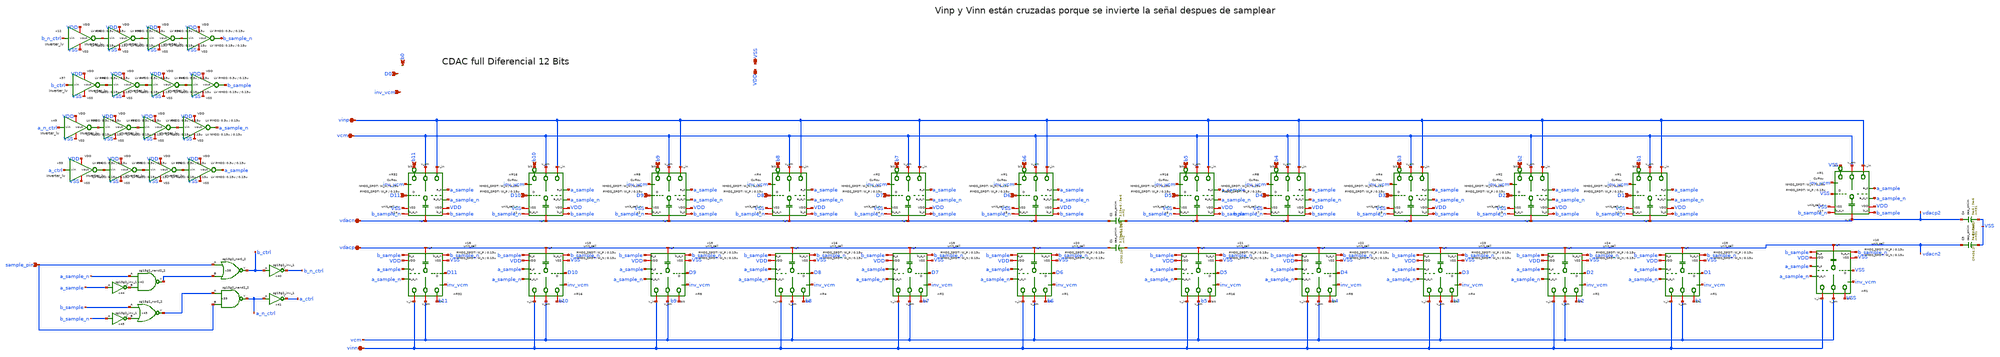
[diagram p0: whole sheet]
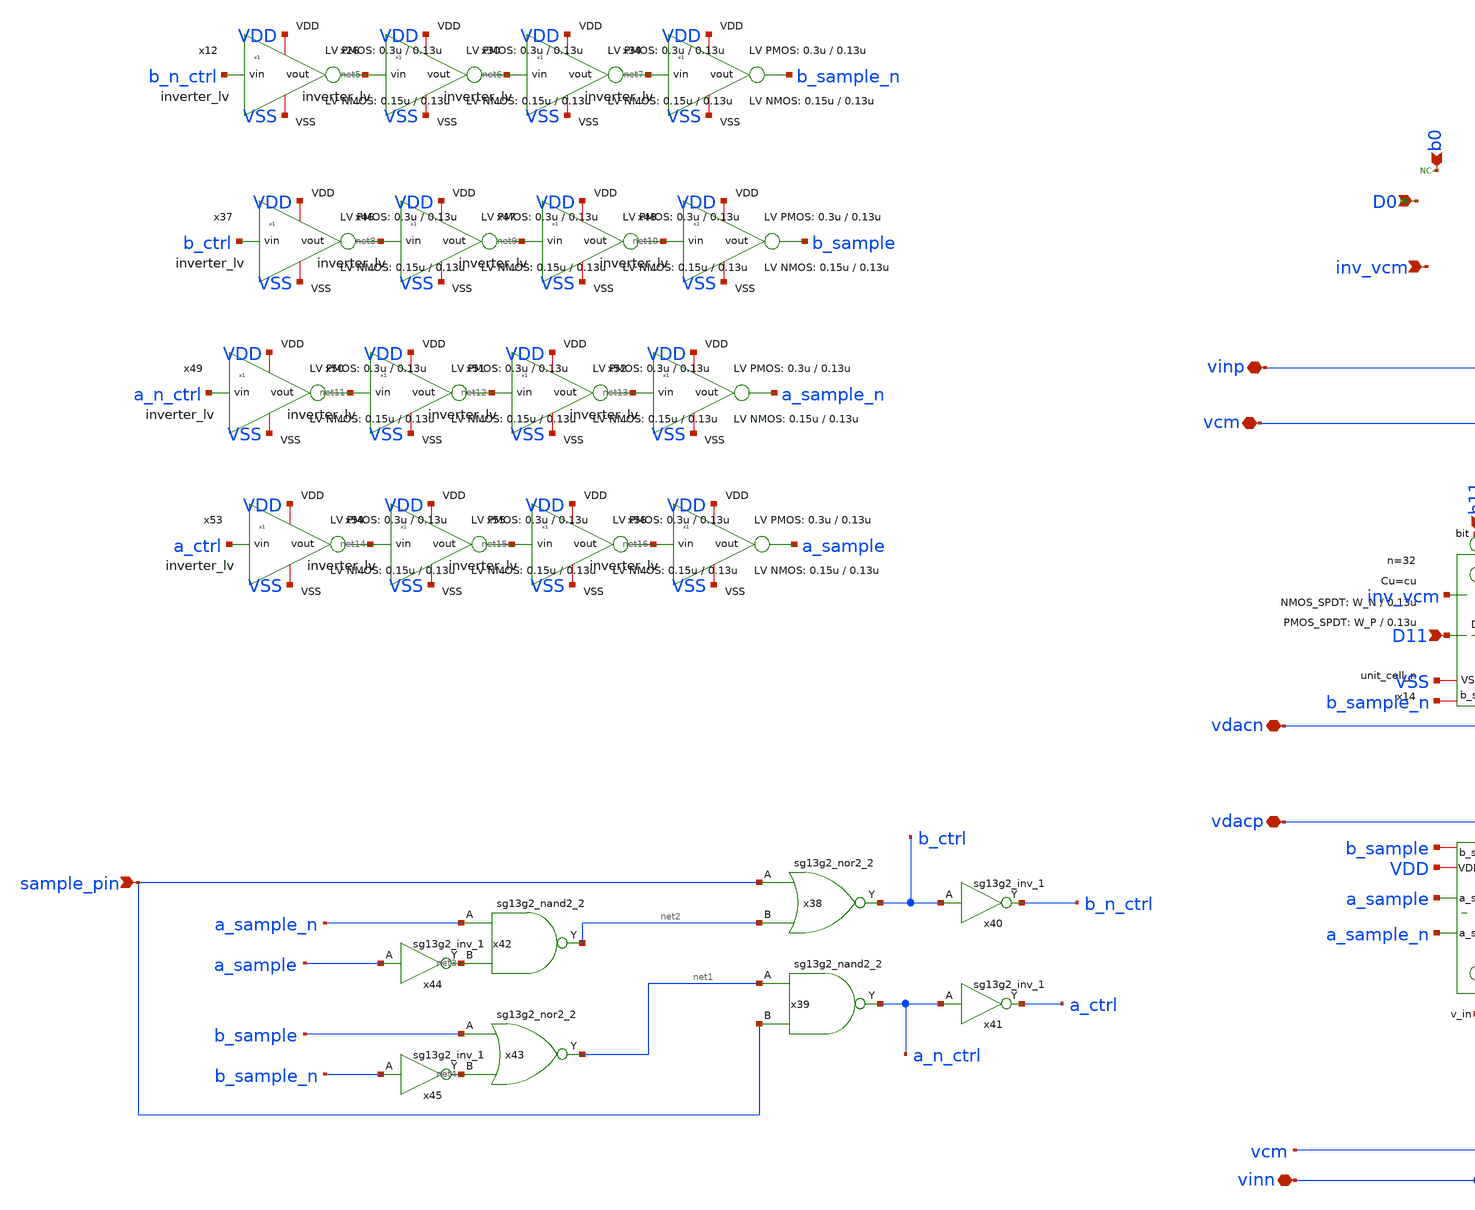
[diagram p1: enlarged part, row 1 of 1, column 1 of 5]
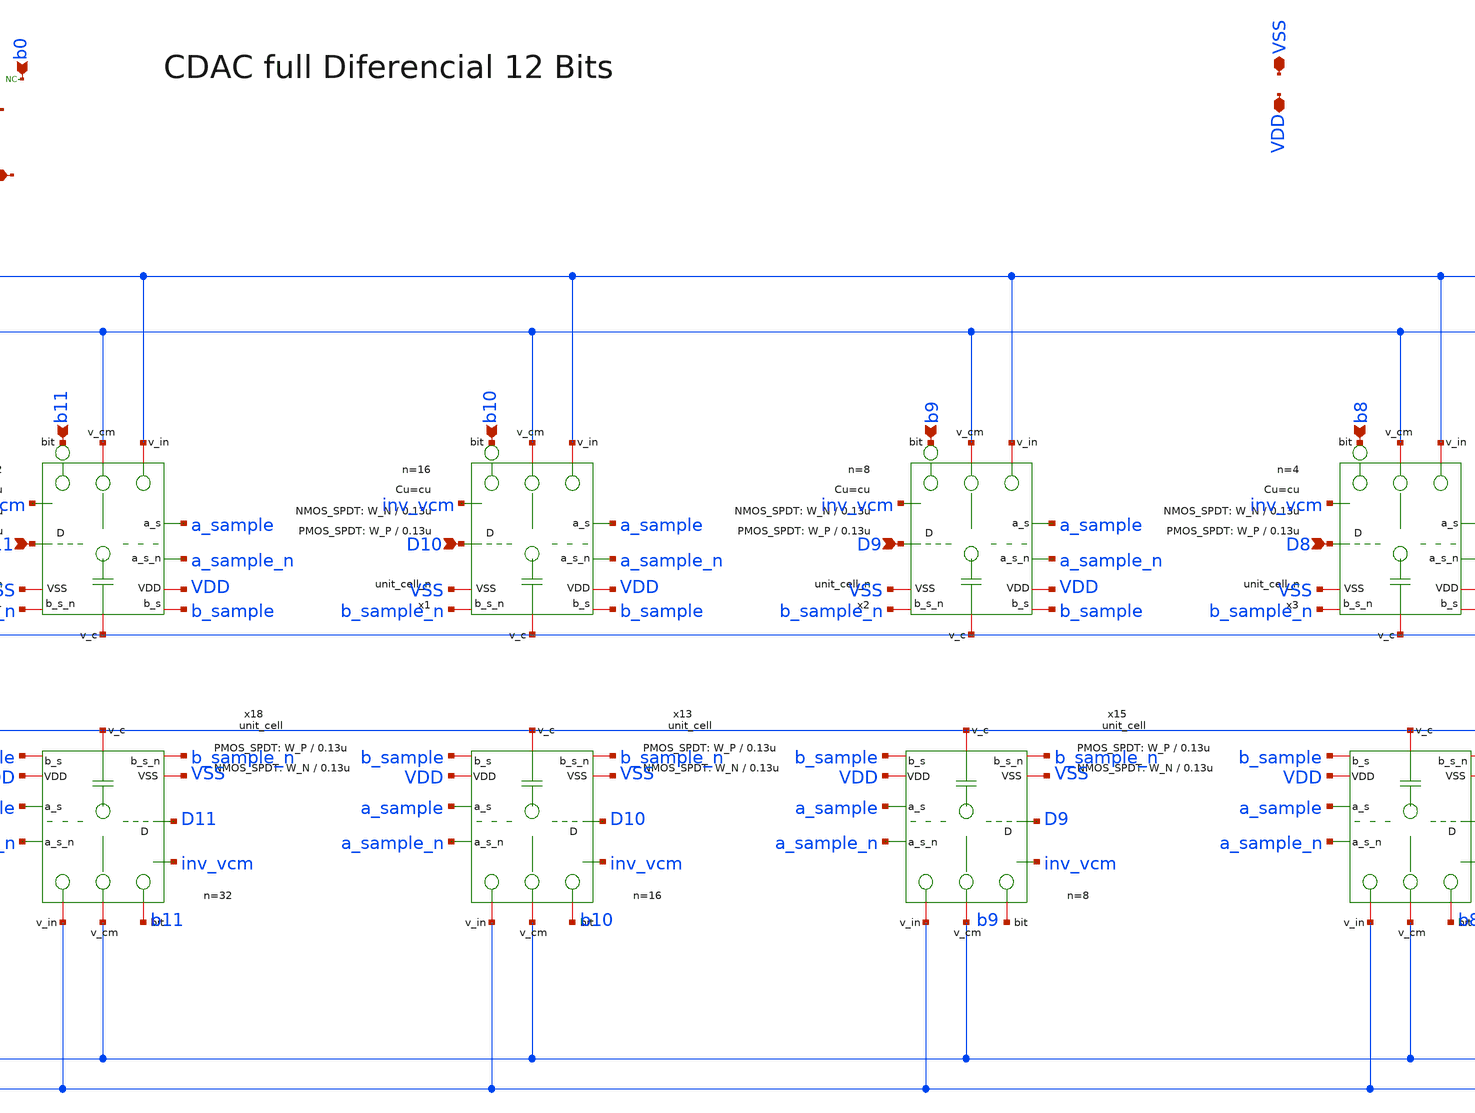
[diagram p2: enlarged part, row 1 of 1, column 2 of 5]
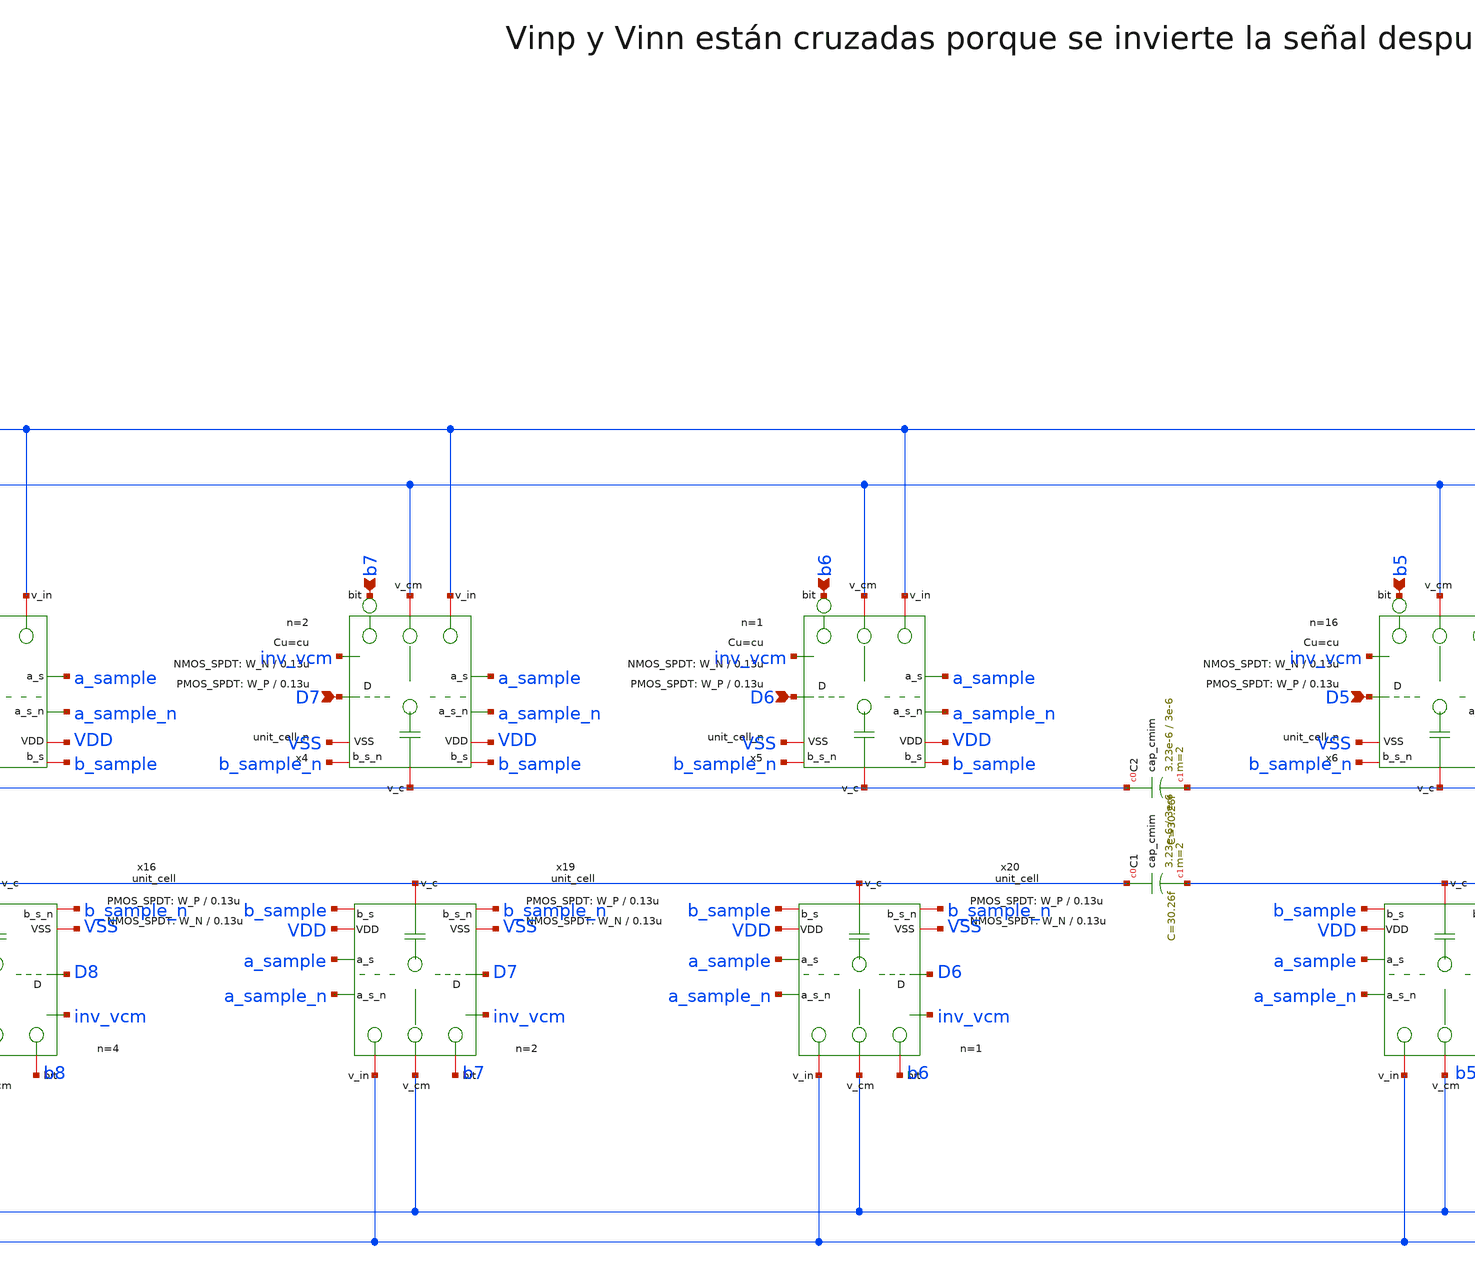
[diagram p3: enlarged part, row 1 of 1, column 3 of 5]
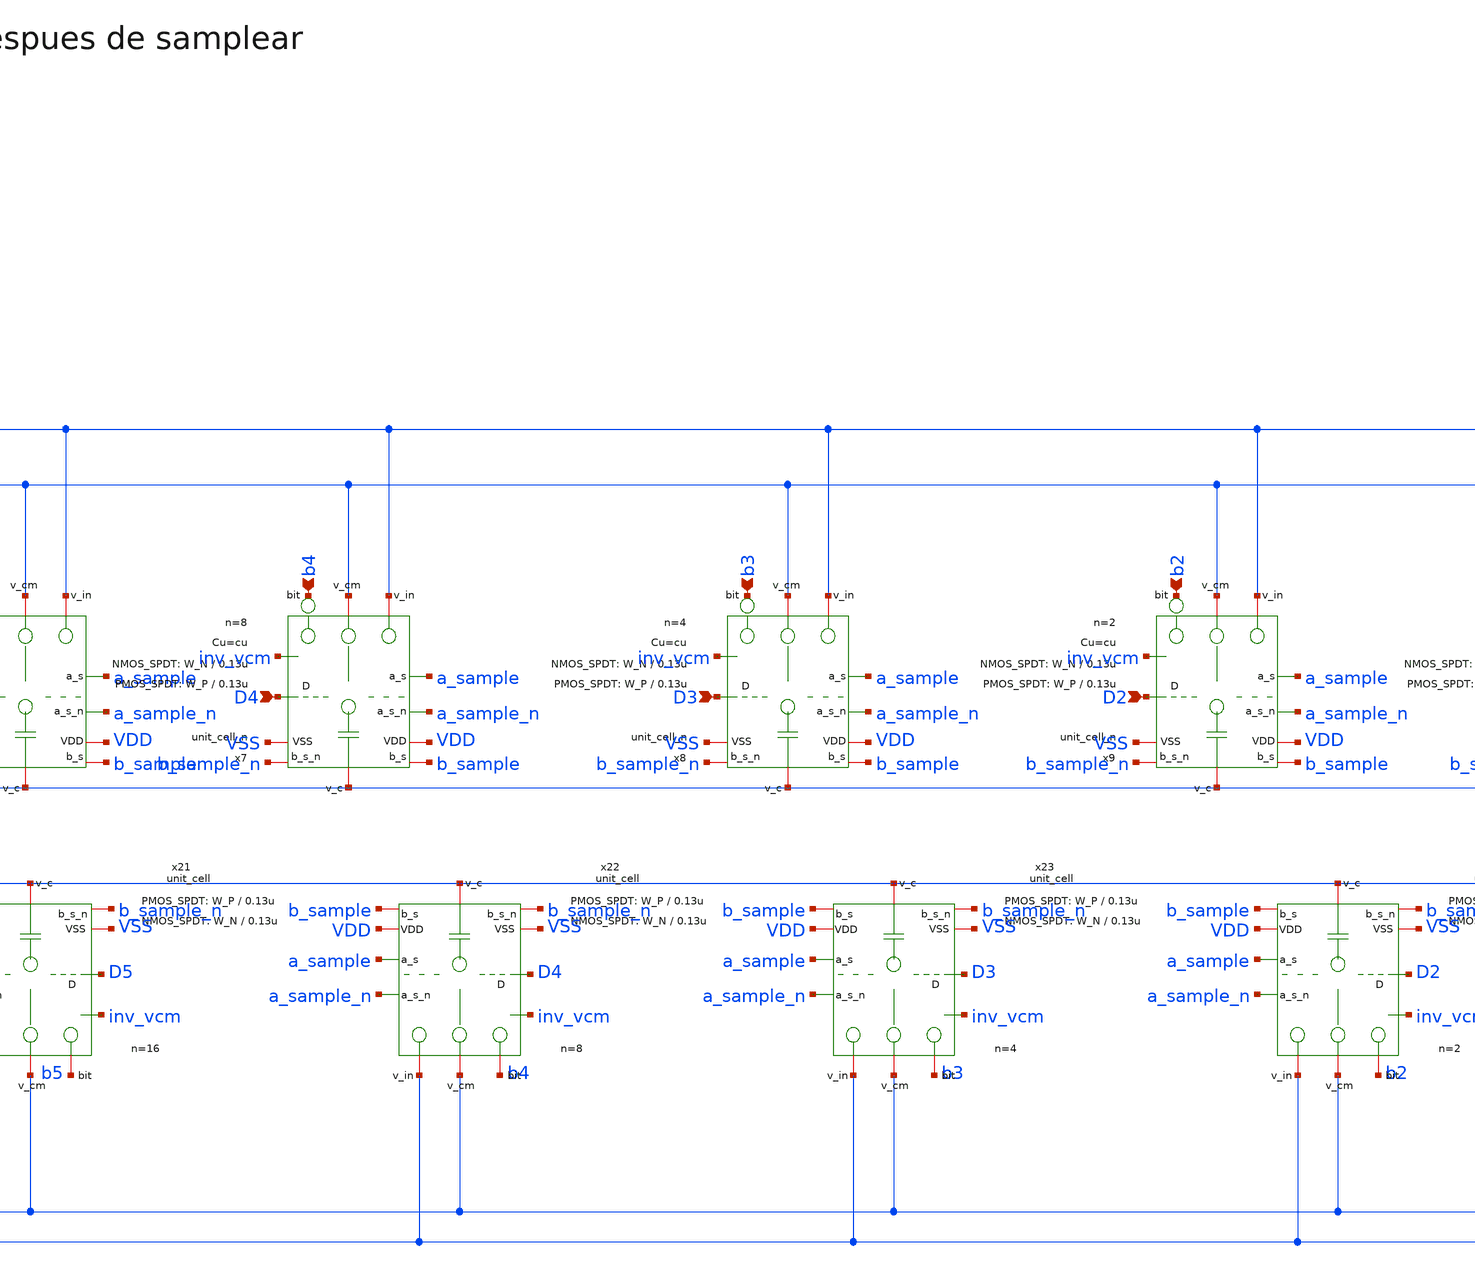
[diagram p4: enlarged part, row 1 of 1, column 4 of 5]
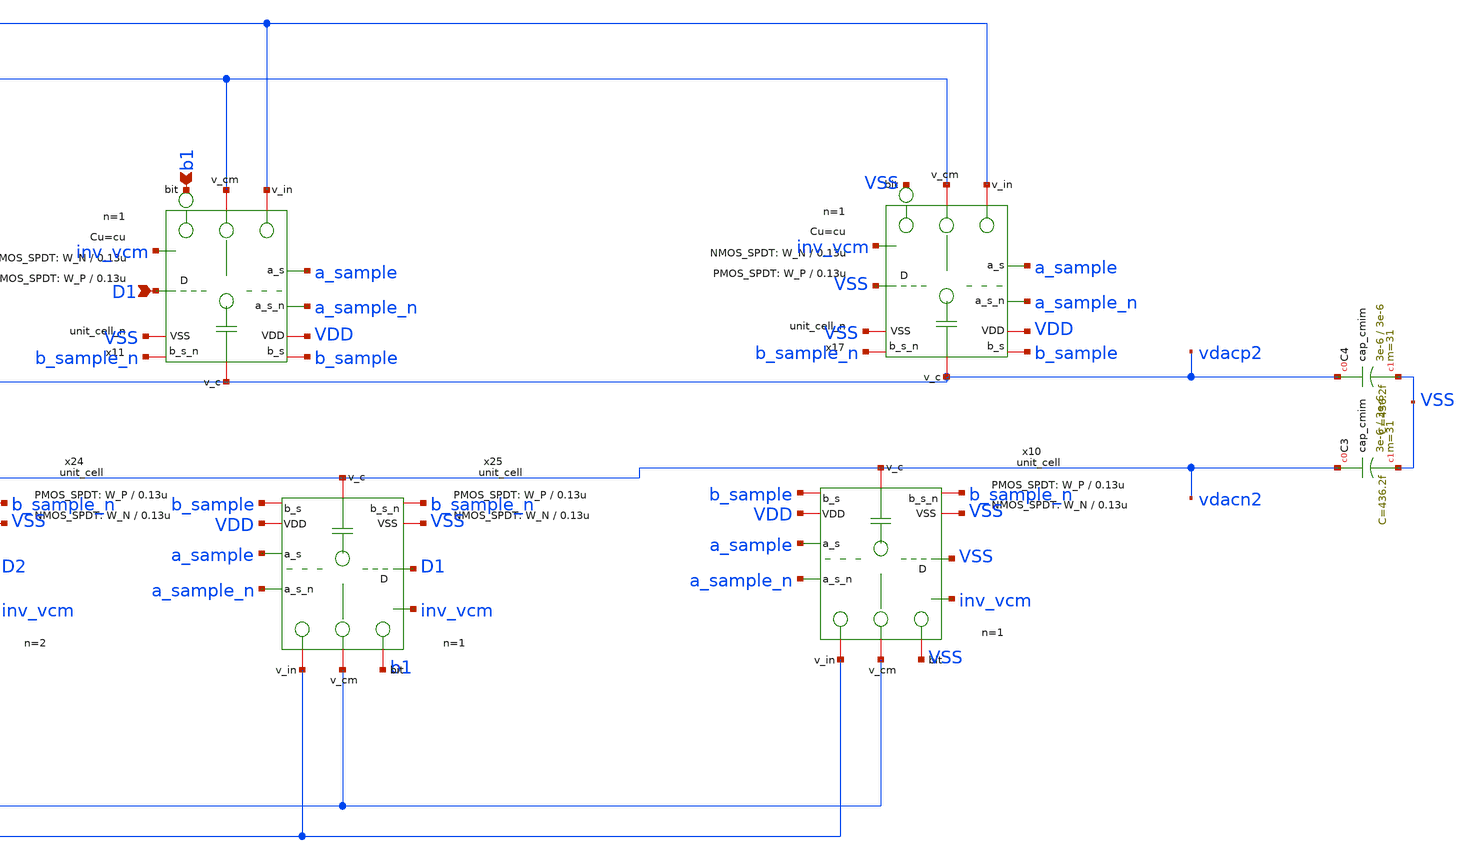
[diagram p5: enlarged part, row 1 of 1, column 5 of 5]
** sch_path: xschem/dac_icms_cell/dac.sch
* IHP-GmbH/IHP-Open-PDK/ihp-sg13g2/libs.tech/xschem/sg13g2_stdcells/sg13g2_nor2_1.sch:
* Copyright 2023 IHP PDK Authors
* Licensed under the Apache License, Version 2.0 (the "License");
**.subckt dac D0 b0 vinn vcm sample_pin vinp vdacp vdacn VSS VDD D1 b1 D2 b2 D3 b3 D4 b4 D5 b5 b6 D7
*+ b7 D8 b8 D9 b9 D10 b10 D11 b11 D6 inv_vcm
*.ipin D0
*.ipin b0
*.iopin vinn
*.iopin vcm
*.ipin sample_pin
*.iopin vinp
*.iopin vdacp
*.iopin vdacn
*.iopin VSS
*.iopin VDD
*.ipin D1
*.ipin b1
*.ipin D2
*.ipin b2
*.ipin D3
*.ipin b3
*.ipin D4
*.ipin b4
*.ipin D5
*.ipin b5
*.ipin b6
*.ipin D7
*.ipin b7
*.ipin D8
*.ipin b8
*.ipin D9
*.ipin b9
*.ipin D10
*.ipin b10
*.ipin D11
*.ipin b11
*.ipin D6
*.ipin inv_vcm
x14 VDD D11 VSS vdacn b11 vcm vinp a_sample a_sample_n b_sample b_sample_n inv_vcm unit_cell_n
+ W_P_SPDT=W_P L_P_SPDT=0.13u W_N_SPDT=W_N L_N_SPDT=0.13u Cu=cu n=32
x18 VDD D11 VSS vdacp b11 vcm vinn a_sample a_sample_n b_sample b_sample_n inv_vcm unit_cell
+ W_P_SPDT=W_P L_P_SPDT=0.13u W_N_SPDT=W_N L_N_SPDT=0.13u Cu=cu n=32
x1 VDD D10 VSS vdacn b10 vcm vinp a_sample a_sample_n b_sample b_sample_n inv_vcm unit_cell_n
+ W_P_SPDT=W_P L_P_SPDT=0.13u W_N_SPDT=W_N L_N_SPDT=0.13u Cu=cu n=16
x2 VDD D9 VSS vdacn b9 vcm vinp a_sample a_sample_n b_sample b_sample_n inv_vcm unit_cell_n
+ W_P_SPDT=W_P L_P_SPDT=0.13u W_N_SPDT=W_N L_N_SPDT=0.13u Cu=cu n=8
x3 VDD D8 VSS vdacn b8 vcm vinp a_sample a_sample_n b_sample b_sample_n inv_vcm unit_cell_n
+ W_P_SPDT=W_P L_P_SPDT=0.13u W_N_SPDT=W_N L_N_SPDT=0.13u Cu=cu n=4
x4 VDD D7 VSS vdacn b7 vcm vinp a_sample a_sample_n b_sample b_sample_n inv_vcm unit_cell_n
+ W_P_SPDT=W_P L_P_SPDT=0.13u W_N_SPDT=W_N L_N_SPDT=0.13u Cu=cu n=2
x5 VDD D6 VSS vdacn b6 vcm vinp a_sample a_sample_n b_sample b_sample_n inv_vcm unit_cell_n
+ W_P_SPDT=W_P L_P_SPDT=0.13u W_N_SPDT=W_N L_N_SPDT=0.13u Cu=cu n=1
x6 VDD D5 VSS vdacp2 b5 vcm vinp a_sample a_sample_n b_sample b_sample_n inv_vcm unit_cell_n
+ W_P_SPDT=W_P L_P_SPDT=0.13u W_N_SPDT=W_N L_N_SPDT=0.13u Cu=cu n=16
x7 VDD D4 VSS vdacp2 b4 vcm vinp a_sample a_sample_n b_sample b_sample_n inv_vcm unit_cell_n
+ W_P_SPDT=W_P L_P_SPDT=0.13u W_N_SPDT=W_N L_N_SPDT=0.13u Cu=cu n=8
x8 VDD D3 VSS vdacp2 b3 vcm vinp a_sample a_sample_n b_sample b_sample_n inv_vcm unit_cell_n
+ W_P_SPDT=W_P L_P_SPDT=0.13u W_N_SPDT=W_N L_N_SPDT=0.13u Cu=cu n=4
x9 VDD D2 VSS vdacp2 b2 vcm vinp a_sample a_sample_n b_sample b_sample_n inv_vcm unit_cell_n
+ W_P_SPDT=W_P L_P_SPDT=0.13u W_N_SPDT=W_N L_N_SPDT=0.13u Cu=cu n=2
x11 VDD D1 VSS vdacp2 b1 vcm vinp a_sample a_sample_n b_sample b_sample_n inv_vcm unit_cell_n
+ W_P_SPDT=W_P L_P_SPDT=0.13u W_N_SPDT=W_N L_N_SPDT=0.13u Cu=cu n=1
x13 VDD D10 VSS vdacp b10 vcm vinn a_sample a_sample_n b_sample b_sample_n inv_vcm unit_cell
+ W_P_SPDT=W_P L_P_SPDT=0.13u W_N_SPDT=W_N L_N_SPDT=0.13u Cu=cu n=16
x15 VDD D9 VSS vdacp b9 vcm vinn a_sample a_sample_n b_sample b_sample_n inv_vcm unit_cell
+ W_P_SPDT=W_P L_P_SPDT=0.13u W_N_SPDT=W_N L_N_SPDT=0.13u Cu=cu n=8
x16 VDD D8 VSS vdacp b8 vcm vinn a_sample a_sample_n b_sample b_sample_n inv_vcm unit_cell
+ W_P_SPDT=W_P L_P_SPDT=0.13u W_N_SPDT=W_N L_N_SPDT=0.13u Cu=cu n=4
x19 VDD D7 VSS vdacp b7 vcm vinn a_sample a_sample_n b_sample b_sample_n inv_vcm unit_cell
+ W_P_SPDT=W_P L_P_SPDT=0.13u W_N_SPDT=W_N L_N_SPDT=0.13u Cu=cu n=2
x20 VDD D6 VSS vdacp b6 vcm vinn a_sample a_sample_n b_sample b_sample_n inv_vcm unit_cell
+ W_P_SPDT=W_P L_P_SPDT=0.13u W_N_SPDT=W_N L_N_SPDT=0.13u Cu=cu n=1
x21 VDD D5 VSS vdacn2 b5 vcm vinn a_sample a_sample_n b_sample b_sample_n inv_vcm unit_cell
+ W_P_SPDT=W_P L_P_SPDT=0.13u W_N_SPDT=W_N L_N_SPDT=0.13u Cu=cu n=16
x22 VDD D4 VSS vdacn2 b4 vcm vinn a_sample a_sample_n b_sample b_sample_n inv_vcm unit_cell
+ W_P_SPDT=W_P L_P_SPDT=0.13u W_N_SPDT=W_N L_N_SPDT=0.13u Cu=cu n=8
x23 VDD D3 VSS vdacn2 b3 vcm vinn a_sample a_sample_n b_sample b_sample_n inv_vcm unit_cell
+ W_P_SPDT=W_P L_P_SPDT=0.13u W_N_SPDT=W_N L_N_SPDT=0.13u Cu=cu n=4
x24 VDD D2 VSS vdacn2 b2 vcm vinn a_sample a_sample_n b_sample b_sample_n inv_vcm unit_cell
+ W_P_SPDT=W_P L_P_SPDT=0.13u W_N_SPDT=W_N L_N_SPDT=0.13u Cu=cu n=2
x25 VDD D1 VSS vdacn2 b1 vcm vinn a_sample a_sample_n b_sample b_sample_n inv_vcm unit_cell
+ W_P_SPDT=W_P L_P_SPDT=0.13u W_N_SPDT=W_N L_N_SPDT=0.13u Cu=cu n=1
x38 b_ctrl sample_pin net2 VDD VSS sg13g2_nor2_2
x39 a_n_ctrl net1 sample_pin VDD VSS sg13g2_nand2_2
x40 b_n_ctrl b_ctrl VDD VSS sg13g2_inv_1
x41 a_ctrl a_n_ctrl VDD VSS sg13g2_inv_1
x42 net2 a_sample_n net3 VDD VSS sg13g2_nand2_2
x43 net1 b_sample net4 VDD VSS sg13g2_nor2_2
x44 net3 a_sample VDD VSS sg13g2_inv_1
x45 net4 b_sample_n VDD VSS sg13g2_inv_1
XC1 vdacp vdacn2 cap_cmim w=3.23e-6 l=3e-6 m=2 mm_ok=1
XC2 vdacn vdacp2 cap_cmim w=3.23e-6 l=3e-6 m=2 mm_ok=1
x10 VDD VSS VSS vdacn2 VSS vcm vinn a_sample a_sample_n b_sample b_sample_n inv_vcm unit_cell
+ W_P_SPDT=W_P L_P_SPDT=0.13u W_N_SPDT=W_N L_N_SPDT=0.13u Cu=cu n=1
x17 VDD VSS VSS vdacp2 VSS vcm vinp a_sample a_sample_n b_sample b_sample_n inv_vcm unit_cell_n
+ W_P_SPDT=W_P L_P_SPDT=0.13u W_N_SPDT=W_N L_N_SPDT=0.13u Cu=cu n=1
XC3 vdacn2 VSS cap_cmim w=3e-6 l=3e-6 m=31 mm_ok=1
XC4 vdacp2 VSS cap_cmim w=3e-6 l=3e-6 m=31 mm_ok=1
* noconn b0
* noconn D0
x12 VDD b_n_ctrl net5 VSS inverter_lv W_P=0.3u L_P=0.13u W_N=0.15u L_N=0.13u N_C=1
x26 VDD net5 net6 VSS inverter_lv W_P=0.3u L_P=0.13u W_N=0.15u L_N=0.13u N_C=1
x30 VDD net6 net7 VSS inverter_lv W_P=0.3u L_P=0.13u W_N=0.15u L_N=0.13u N_C=1
x34 VDD net7 b_sample_n VSS inverter_lv W_P=0.3u L_P=0.13u W_N=0.15u L_N=0.13u N_C=1
x37 VDD b_ctrl net8 VSS inverter_lv W_P=0.3u L_P=0.13u W_N=0.15u L_N=0.13u N_C=1
x46 VDD net8 net9 VSS inverter_lv W_P=0.3u L_P=0.13u W_N=0.15u L_N=0.13u N_C=1
x47 VDD net9 net10 VSS inverter_lv W_P=0.3u L_P=0.13u W_N=0.15u L_N=0.13u N_C=1
x48 VDD net10 b_sample VSS inverter_lv W_P=0.3u L_P=0.13u W_N=0.15u L_N=0.13u N_C=1
x49 VDD a_n_ctrl net11 VSS inverter_lv W_P=0.3u L_P=0.13u W_N=0.15u L_N=0.13u N_C=1
x50 VDD net11 net12 VSS inverter_lv W_P=0.3u L_P=0.13u W_N=0.15u L_N=0.13u N_C=1
x51 VDD net12 net13 VSS inverter_lv W_P=0.3u L_P=0.13u W_N=0.15u L_N=0.13u N_C=1
x52 VDD net13 a_sample_n VSS inverter_lv W_P=0.3u L_P=0.13u W_N=0.15u L_N=0.13u N_C=1
x53 VDD a_ctrl net14 VSS inverter_lv W_P=0.3u L_P=0.13u W_N=0.15u L_N=0.13u N_C=1
x54 VDD net14 net15 VSS inverter_lv W_P=0.3u L_P=0.13u W_N=0.15u L_N=0.13u N_C=1
x55 VDD net15 net16 VSS inverter_lv W_P=0.3u L_P=0.13u W_N=0.15u L_N=0.13u N_C=1
x56 VDD net16 a_sample VSS inverter_lv W_P=0.3u L_P=0.13u W_N=0.15u L_N=0.13u N_C=1
**.ends

* expanding   symbol:  dac_icms_cell/unit_cell_n.sym # of pins=12
** sym_path: xschem/dac_icms_cell/unit_cell_n.sym
** sch_path: xschem/dac_icms_cell/unit_cell_n.sch
.subckt unit_cell_n VDD d VSS v_top bit v_cm v_in a_sample a_sample_n b_sample b_sample_n inv_vcm
+  W_P_SPDT=1.0u L_P_SPDT=0.13u W_N_SPDT=1.0u L_N_SPDT=0.13u Cu=8f n=1
*.iopin v_top
*.ipin a_sample
*.ipin a_sample_n
*.ipin b_sample
*.ipin b_sample_n
*.iopin v_in
*.ipin d
*.iopin v_cm
*.ipin bit
*.ipin inv_vcm
*.iopin VSS
*.iopin VDD
x2 VDD a_sample VSS v_top v_cm a_sample_n transmission_gate_lv_wo_dummy W_P=W_P_SPDT L_P=L_P_SPDT
+ W_N=W_N_SPDT L_N=L_N_SPDT W_P_D=1.0u L_P_D=0.13u W_N_D=1.0u L_N_D=0.13u n=n
XC1 TOP_C v_top cap_cmim w=3e-6 l=3e-6 m=n mm_ok=1
XM1 TOP_C n_ctrl VSS VSS sg13_lv_nmos w=1u l=0.13u ng=1 m=n mm_ok=1
XM3 TOP_C p_ctrl VDD VDD sg13_lv_pmos w=2u l=0.13u ng=1 m=n mm_ok=1
x3 VDD tg_vcm_ctrl VSS TOP_C v_cm tg_vcm_ctrl_n transmission_gate_lv_wo_dummy W_P=W_P_SPDT
+ L_P=L_P_SPDT W_N=W_N_SPDT L_N=L_N_SPDT W_P_D=1.0u L_P_D=0.13u W_N_D=1.0u L_N_D=0.13u n=n
x4 VDD b_sample_n VSS TOP_C v_in b_sample transmission_gate_lv_w_dummy W_P=W_P_SPDT L_P=L_P_SPDT
+ W_N=W_N_SPDT L_N=L_N_SPDT W_P_D=1.0u L_P_D=0.13u W_N_D=1.0u L_N_D=0.13u n=n
x23 p_ctrl_1 bit d VDD VSS sg13g2_and2_1
x46 n_ctrl_1 bit_n d VDD VSS sg13g2_nand2_1
x32 bit_n bit VDD VSS sg13g2_inv_1
x1 tg_vcm_ctrl_1 d b_sample_n VDD VSS sg13g2_or2_1
x8 tg_vcm_ctrl_n_1 d b_sample_n VDD VSS sg13g2_nor2_1
x10 VDD p_ctrl_2 p_ctrl_3 VSS inverter_lv W_P=0.3u L_P=0.13u W_N=0.15u L_N=0.13u N_C=1
x5 VDD p_ctrl_1 p_ctrl_2 VSS inverter_lv W_P=0.3u L_P=0.13u W_N=0.15u L_N=0.13u N_C=1
x6 VDD p_ctrl_3 p_ctrl VSS inverter_lv W_P=0.3u L_P=0.13u W_N=0.15u L_N=0.13u N_C=1
x11 VDD n_ctrl_2 n_ctrl_3 VSS inverter_lv W_P=0.3u L_P=0.13u W_N=0.15u L_N=0.13u N_C=1
x12 VDD n_ctrl_1 n_ctrl_2 VSS inverter_lv W_P=0.3u L_P=0.13u W_N=0.15u L_N=0.13u N_C=1
x13 VDD n_ctrl_3 n_ctrl VSS inverter_lv W_P=0.3u L_P=0.13u W_N=0.15u L_N=0.13u N_C=1
x7 VDD tg_vcm_ctrl_2 tg_vcm_ctrl_3 VSS inverter_lv W_P=0.3u L_P=0.13u W_N=0.15u L_N=0.13u N_C=1
x9 VDD tg_vcm_ctrl_1 tg_vcm_ctrl_2 VSS inverter_lv W_P=0.3u L_P=0.13u W_N=0.15u L_N=0.13u N_C=1
x14 VDD tg_vcm_ctrl_3 tg_vcm_ctrl VSS inverter_lv W_P=0.3u L_P=0.13u W_N=0.15u L_N=0.13u N_C=1
x15 VDD tg_vcm_ctrl_n_2 tg_vcm_ctrl_n_3 VSS inverter_lv W_P=0.3u L_P=0.13u W_N=0.15u L_N=0.13u N_C=1
x16 VDD tg_vcm_ctrl_n_1 tg_vcm_ctrl_n_2 VSS inverter_lv W_P=0.3u L_P=0.13u W_N=0.15u L_N=0.13u N_C=1
x17 VDD tg_vcm_ctrl_n_3 tg_vcm_ctrl_n VSS inverter_lv W_P=0.3u L_P=0.13u W_N=0.15u L_N=0.13u N_C=1
.ends


* expanding   symbol:  dac_icms_cell/unit_cell.sym # of pins=12
** sym_path: xschem/dac_icms_cell/unit_cell.sym
** sch_path: xschem/dac_icms_cell/unit_cell.sch
.subckt unit_cell VDD d VSS v_top bit v_cm v_in a_sample a_sample_n b_sample b_sample_n inv_vcm
+  W_P_SPDT=1.0u L_P_SPDT=0.13u W_N_SPDT=1.0u L_N_SPDT=0.13u Cu=8f n=1
*.iopin v_top
*.ipin a_sample
*.ipin a_sample_n
*.ipin b_sample
*.ipin b_sample_n
*.iopin v_in
*.ipin d
*.iopin v_cm
*.ipin bit
*.ipin inv_vcm
*.iopin VSS
*.iopin VDD
x2 VDD a_sample VSS v_top v_cm a_sample_n transmission_gate_lv_wo_dummy W_P=W_P_SPDT L_P=L_P_SPDT
+ W_N=W_N_SPDT L_N=L_N_SPDT W_P_D=1.0u L_P_D=0.13u W_N_D=1.0u L_N_D=0.13u n=n
XC1 TOP_C v_top cap_cmim w=3e-6 l=3e-6 m=n mm_ok=1
XM1 TOP_C n_ctrl VSS VSS sg13_lv_nmos w=1u l=0.13u ng=1 m=n mm_ok=1
XM3 TOP_C p_ctrl VDD VDD sg13_lv_pmos w=2u l=0.13u ng=1 m=n mm_ok=1
x3 VDD tg_vcm_ctrl VSS TOP_C v_cm tg_vcm_ctrl_n transmission_gate_lv_wo_dummy W_P=W_P_SPDT
+ L_P=L_P_SPDT W_N=W_N_SPDT L_N=L_N_SPDT W_P_D=1.0u L_P_D=0.13u W_N_D=1.0u L_N_D=0.13u n=n
x4 VDD b_sample_n VSS TOP_C v_in b_sample transmission_gate_lv_w_dummy W_P=W_P_SPDT L_P=L_P_SPDT
+ W_N=W_N_SPDT L_N=L_N_SPDT W_P_D=1.0u L_P_D=0.13u W_N_D=1.0u L_N_D=0.13u n=n
x23 p_ctrl_1 bit_n d VDD VSS sg13g2_and2_1
x46 n_ctrl_1 bit d VDD VSS sg13g2_nand2_1
x32 bit_n bit VDD VSS sg13g2_inv_1
x1 tg_vcm_ctrl_1 d b_sample_n VDD VSS sg13g2_or2_1
x8 tg_vcm_ctrl_n_1 d b_sample_n VDD VSS sg13g2_nor2_1
x10 VDD p_ctrl_2 p_ctrl_3 VSS inverter_lv W_P=0.3u L_P=0.13u W_N=0.15u L_N=0.13u N_C=1
x5 VDD p_ctrl_1 p_ctrl_2 VSS inverter_lv W_P=0.3u L_P=0.13u W_N=0.15u L_N=0.13u N_C=1
x6 VDD p_ctrl_3 p_ctrl VSS inverter_lv W_P=0.3u L_P=0.13u W_N=0.15u L_N=0.13u N_C=1
x11 VDD n_ctrl_2 n_ctrl_3 VSS inverter_lv W_P=0.3u L_P=0.13u W_N=0.15u L_N=0.13u N_C=1
x12 VDD n_ctrl_1 n_ctrl_2 VSS inverter_lv W_P=0.3u L_P=0.13u W_N=0.15u L_N=0.13u N_C=1
x13 VDD n_ctrl_3 n_ctrl VSS inverter_lv W_P=0.3u L_P=0.13u W_N=0.15u L_N=0.13u N_C=1
x7 VDD tg_vcm_ctrl_2 tg_vcm_ctrl_3 VSS inverter_lv W_P=0.3u L_P=0.13u W_N=0.15u L_N=0.13u N_C=1
x9 VDD tg_vcm_ctrl_1 tg_vcm_ctrl_2 VSS inverter_lv W_P=0.3u L_P=0.13u W_N=0.15u L_N=0.13u N_C=1
x14 VDD tg_vcm_ctrl_3 tg_vcm_ctrl VSS inverter_lv W_P=0.3u L_P=0.13u W_N=0.15u L_N=0.13u N_C=1
x15 VDD tg_vcm_ctrl_n_2 tg_vcm_ctrl_n_3 VSS inverter_lv W_P=0.3u L_P=0.13u W_N=0.15u L_N=0.13u N_C=1
x16 VDD tg_vcm_ctrl_n_1 tg_vcm_ctrl_n_2 VSS inverter_lv W_P=0.3u L_P=0.13u W_N=0.15u L_N=0.13u N_C=1
x17 VDD tg_vcm_ctrl_n_3 tg_vcm_ctrl_n VSS inverter_lv W_P=0.3u L_P=0.13u W_N=0.15u L_N=0.13u N_C=1
.ends


* expanding   symbol:  sg13g2_stdcells/sg13g2_nor2_2.sym # of pins=3
** sym_path: sg13g2_stdcells/sg13g2_nor2_2.sym
** sch_path: sg13g2_stdcells/sg13g2_nor2_2.sch
.subckt sg13g2_nor2_2 Y A B VDD VSS
*.opin Y
*.ipin B
*.ipin A
*.iopin VDD
*.iopin VSS
XM1 Y A VSS VSS sg13_lv_nmos w=1.48u l=130.00n ng=2 m=1 mm_ok=1
XM2 Y B VSS VSS sg13_lv_nmos w=1.48u l=130.00n ng=2 m=1 mm_ok=1
XM3 net1 A VDD VDD sg13_lv_pmos w=2.24u l=130.00n ng=2 m=1 mm_ok=1
XM4 Y B net1 VDD sg13_lv_pmos w=2.24u l=130.00n ng=2 m=1 mm_ok=1
.ends


* expanding   symbol:  sg13g2_stdcells/sg13g2_nand2_2.sym # of pins=3
** sym_path: sg13g2_stdcells/sg13g2_nand2_2.sym
** sch_path: sg13g2_stdcells/sg13g2_nand2_2.sch
.subckt sg13g2_nand2_2 Y A B VDD VSS
*.iopin VDD
*.iopin VSS
*.opin Y
*.ipin B
*.ipin A
XM1 Y A net1 VSS sg13_lv_nmos w=1.44u l=130.00n ng=2 m=1 mm_ok=1
XM2 net1 B VSS VSS sg13_lv_nmos w=1.44u l=130.00n ng=2 m=1 mm_ok=1
XM3 Y A VDD VDD sg13_lv_pmos w=2.24u l=130.00n ng=2 m=1 mm_ok=1
XM4 Y B VDD VDD sg13_lv_pmos w=2.24u l=130.00n ng=2 m=1 mm_ok=1
.ends


* expanding   symbol:  sg13g2_stdcells/sg13g2_inv_1.sym # of pins=2
** sym_path: sg13g2_stdcells/sg13g2_inv_1.sym
** sch_path: sg13g2_stdcells/sg13g2_inv_1.sch
.subckt sg13g2_inv_1 Y A VDD VSS
*.opin Y
*.ipin A
*.iopin VDD
*.iopin VSS
XM1 Y A VSS VSS sg13_lv_nmos w=740.00n l=130.00n ng=1 m=1 mm_ok=1
XM2 Y A VDD VDD sg13_lv_pmos w=1.12u l=130.00n ng=1 m=1 mm_ok=1
.ends


* expanding   symbol:  inverter/inverter_lv.sym # of pins=4
** sym_path: xschem/inverter/inverter_lv.sym
** sch_path: xschem/inverter/inverter_lv.sch
.subckt inverter_lv VDD vin vout VSS  W_P=3.0u L_P=0.13u W_N=1.0u L_N=0.13u N_C=1
*.ipin vin
*.iopin VDD
*.iopin VSS
*.opin vout
XM1 vout vin VDD VDD sg13_lv_pmos w=W_P l=L_P ng=1 m={N_C} mm_ok=1
XM2 vout vin VSS VSS sg13_lv_nmos w=W_N l=L_N ng=1 m={N_C} mm_ok=1
.ends


* expanding   symbol:  transmission_gate/transmission_gate_lv_wo_dummy.sym # of pins=6
** sym_path: xschem/transmission_gate/transmission_gate_lv_wo_dummy.sym
** sch_path: xschem/transmission_gate/transmission_gate_lv_wo_dummy.sch
.subckt transmission_gate_lv_wo_dummy VDD di_tg_ctrl VSS v_b v_a di_tg_ctrl_n  W_P=2.0u L_P=0.13u
+ W_N=2.0u L_N=0.13u W_P_D=1.0u L_P_D=0.13u W_N_D=1.0u L_N_D=0.13u n=1
*.iopin v_a
*.iopin v_b
*.iopin VDD
*.iopin VSS
*.ipin di_tg_ctrl
*.ipin di_tg_ctrl_n
XM1 v_a di_tg_ctrl v_b VSS sg13_lv_nmos w=W_N l=L_N ng=1 m=n mm_ok=1
XM2 v_a di_tg_ctrl_n v_b VDD sg13_lv_pmos w=W_P l=L_P ng=1 m=n mm_ok=1
.ends


* expanding   symbol:  transmission_gate/transmission_gate_lv_w_dummy.sym # of pins=6
** sym_path: xschem/transmission_gate/transmission_gate_lv_w_dummy.sym
** sch_path: xschem/transmission_gate/transmission_gate_lv_w_dummy.sch
.subckt transmission_gate_lv_w_dummy VDD di_tg_ctrl VSS v_b v_a di_tg_ctrl_n  W_P=2.0u L_P=0.13u
+ W_N=2.0u L_N=0.13u W_P_D=1.0u L_P_D=0.13u W_N_D=1.0u L_N_D=0.13u n=1
*.iopin v_a
*.iopin v_b
*.iopin VDD
*.iopin VSS
*.ipin di_tg_ctrl
*.ipin di_tg_ctrl_n
XM1 v_a di_tg_ctrl v_b VSS sg13_lv_nmos w=W_N l=L_N ng=1 m=n mm_ok=1
XM2 v_a di_tg_ctrl_n v_b VDD sg13_lv_pmos w=W_P l=L_P ng=1 m=n mm_ok=1
XMdummy2 v_b di_tg_ctrl v_b VDD sg13_lv_pmos w=W_P l=L_P ng=1 m={n/2} mm_ok=1
XMdummy1 v_b di_tg_ctrl_n v_b VSS sg13_lv_nmos w=W_N l=L_N ng=1 m={n/2} mm_ok=1
.ends


* expanding   symbol:  sg13g2_stdcells/sg13g2_and2_1.sym # of pins=3
** sym_path: sg13g2_stdcells/sg13g2_and2_1.sym
** sch_path: sg13g2_stdcells/sg13g2_and2_1.sch
.subckt sg13g2_and2_1 X A B VDD VSS
*.ipin A
*.ipin B
*.opin X
*.iopin VDD
*.iopin VSS
XM1 net1 A net2 VSS sg13_lv_nmos w=640.00n l=130.00n ng=1 m=1 mm_ok=1
XM2 net2 B VSS VSS sg13_lv_nmos w=640.00n l=130.00n ng=1 m=1 mm_ok=1
XM3 X net1 VSS VSS sg13_lv_nmos w=740.00n l=130.00n ng=1 m=1 mm_ok=1
XM4 net1 B VDD VDD sg13_lv_pmos w=840.00n l=130.00n ng=1 m=1 mm_ok=1
XM5 net1 A VDD VDD sg13_lv_pmos w=840.00n l=130.00n ng=1 m=1 mm_ok=1
XM6 X net1 VDD VDD sg13_lv_pmos w=1.12u l=130.00n ng=1 m=1 mm_ok=1
.ends


* expanding   symbol:  sg13g2_stdcells/sg13g2_nand2_1.sym # of pins=3
** sym_path: sg13g2_stdcells/sg13g2_nand2_1.sym
** sch_path: sg13g2_stdcells/sg13g2_nand2_1.sch
.subckt sg13g2_nand2_1 Y A B VDD VSS
*.iopin VDD
*.iopin VSS
*.ipin A
*.ipin B
*.opin Y
XM1 Y A net1 VSS sg13_lv_nmos w=740.00n l=130.00n ng=1 m=1 mm_ok=1
XM2 net1 B VSS VSS sg13_lv_nmos w=740.00n l=130.00n ng=1 m=1 mm_ok=1
XM3 Y A VDD VDD sg13_lv_pmos w=1.12u l=130.00n ng=1 m=1 mm_ok=1
XM4 Y B VDD VDD sg13_lv_pmos w=1.12u l=130.00n ng=1 m=1 mm_ok=1
.ends


* expanding   symbol:  sg13g2_stdcells/sg13g2_or2_1.sym # of pins=3
** sym_path: sg13g2_stdcells/sg13g2_or2_1.sym
** sch_path: sg13g2_stdcells/sg13g2_or2_1.sch
.subckt sg13g2_or2_1 X A B VDD VSS
*.opin X
*.ipin B
*.ipin A
*.iopin VDD
*.iopin VSS
XM1 net1 B VSS VSS sg13_lv_nmos w=550.00n l=130.00n ng=1 m=1 mm_ok=1
XM2 net1 A VSS VSS sg13_lv_nmos w=550.00n l=130.00n ng=1 m=1 mm_ok=1
XM3 X net1 VSS VSS sg13_lv_nmos w=740.00n l=130.00n ng=1 m=1 mm_ok=1
XM4 net2 A VDD VDD sg13_lv_pmos w=840.00n l=130.00n ng=1 m=1 mm_ok=1
XM5 net1 B net2 VDD sg13_lv_pmos w=840.00n l=130.00n ng=1 m=1 mm_ok=1
XM6 X net1 VDD VDD sg13_lv_pmos w=1.12u l=130.00n ng=1 m=1 mm_ok=1
.ends


* expanding   symbol:  sg13g2_stdcells/sg13g2_nor2_1.sym # of pins=3
** sym_path: sg13g2_stdcells/sg13g2_nor2_1.sym
** sch_path: sg13g2_stdcells/sg13g2_nor2_1.sch
.subckt sg13g2_nor2_1 Y A B VDD VSS
*.opin Y
*.ipin B
*.ipin A
*.iopin VDD
*.iopin VSS
XM1 Y A VSS VSS sg13_lv_nmos w=740.00n l=130.00n ng=1 m=1 mm_ok=1
XM2 Y B VSS VSS sg13_lv_nmos w=740.00n l=130.00n ng=1 m=1 mm_ok=1
XM3 net1 A VDD VDD sg13_lv_pmos w=1.12u l=130.00n ng=1 m=1 mm_ok=1
XM4 Y B net1 VDD sg13_lv_pmos w=1.12u l=130.00n ng=1 m=1 mm_ok=1
.ends

.end
